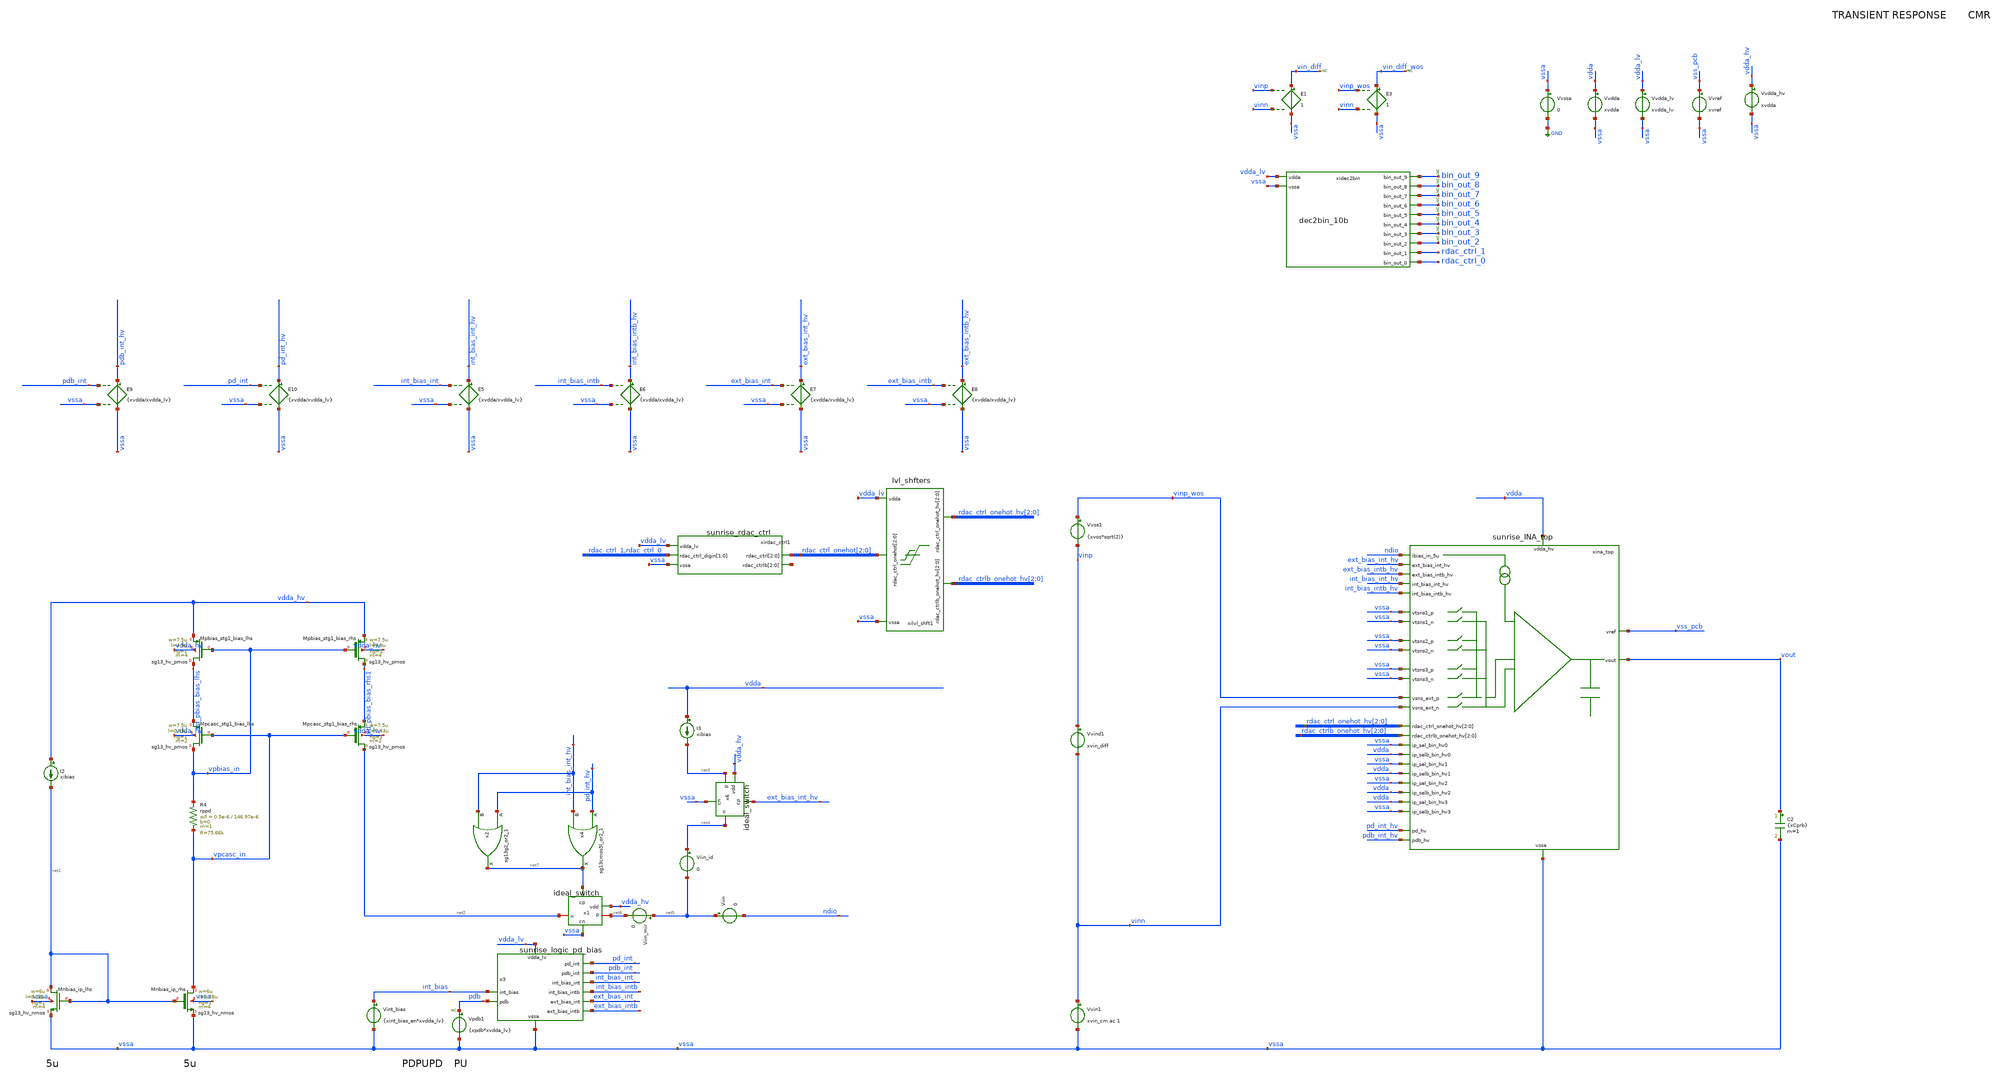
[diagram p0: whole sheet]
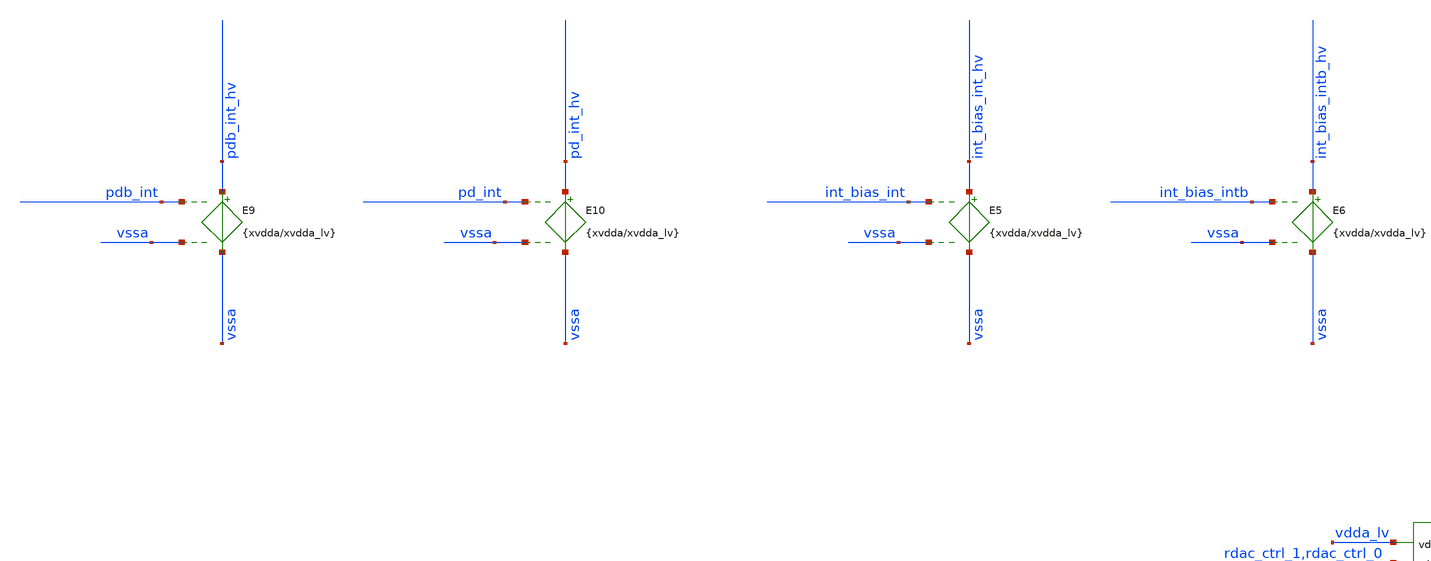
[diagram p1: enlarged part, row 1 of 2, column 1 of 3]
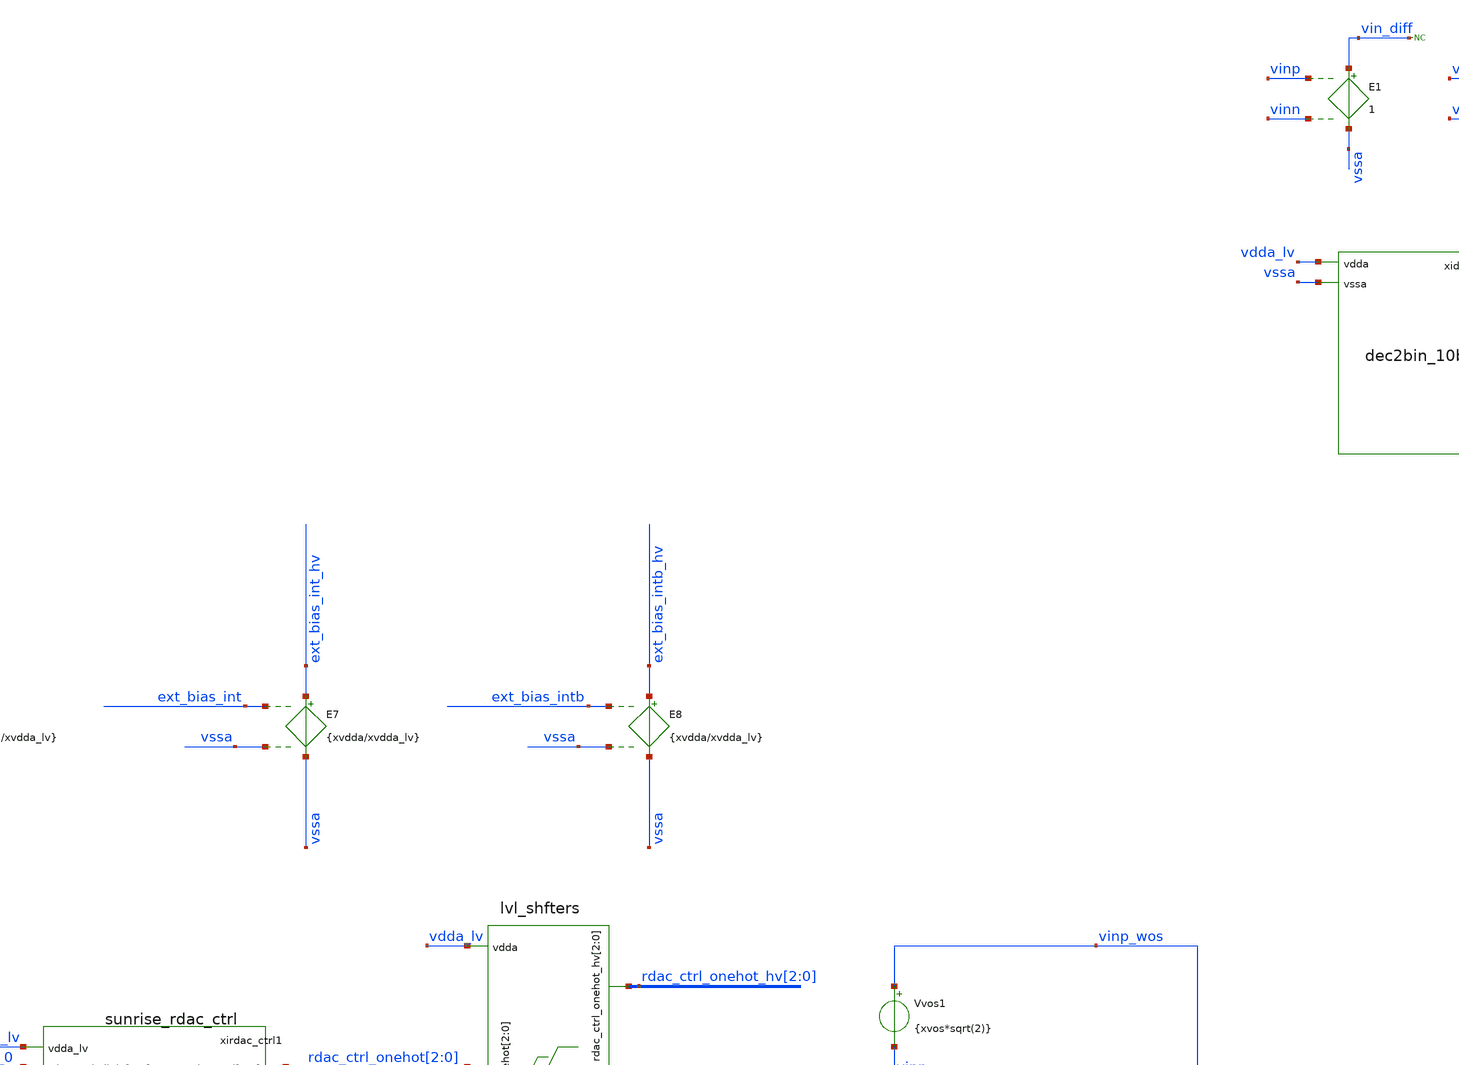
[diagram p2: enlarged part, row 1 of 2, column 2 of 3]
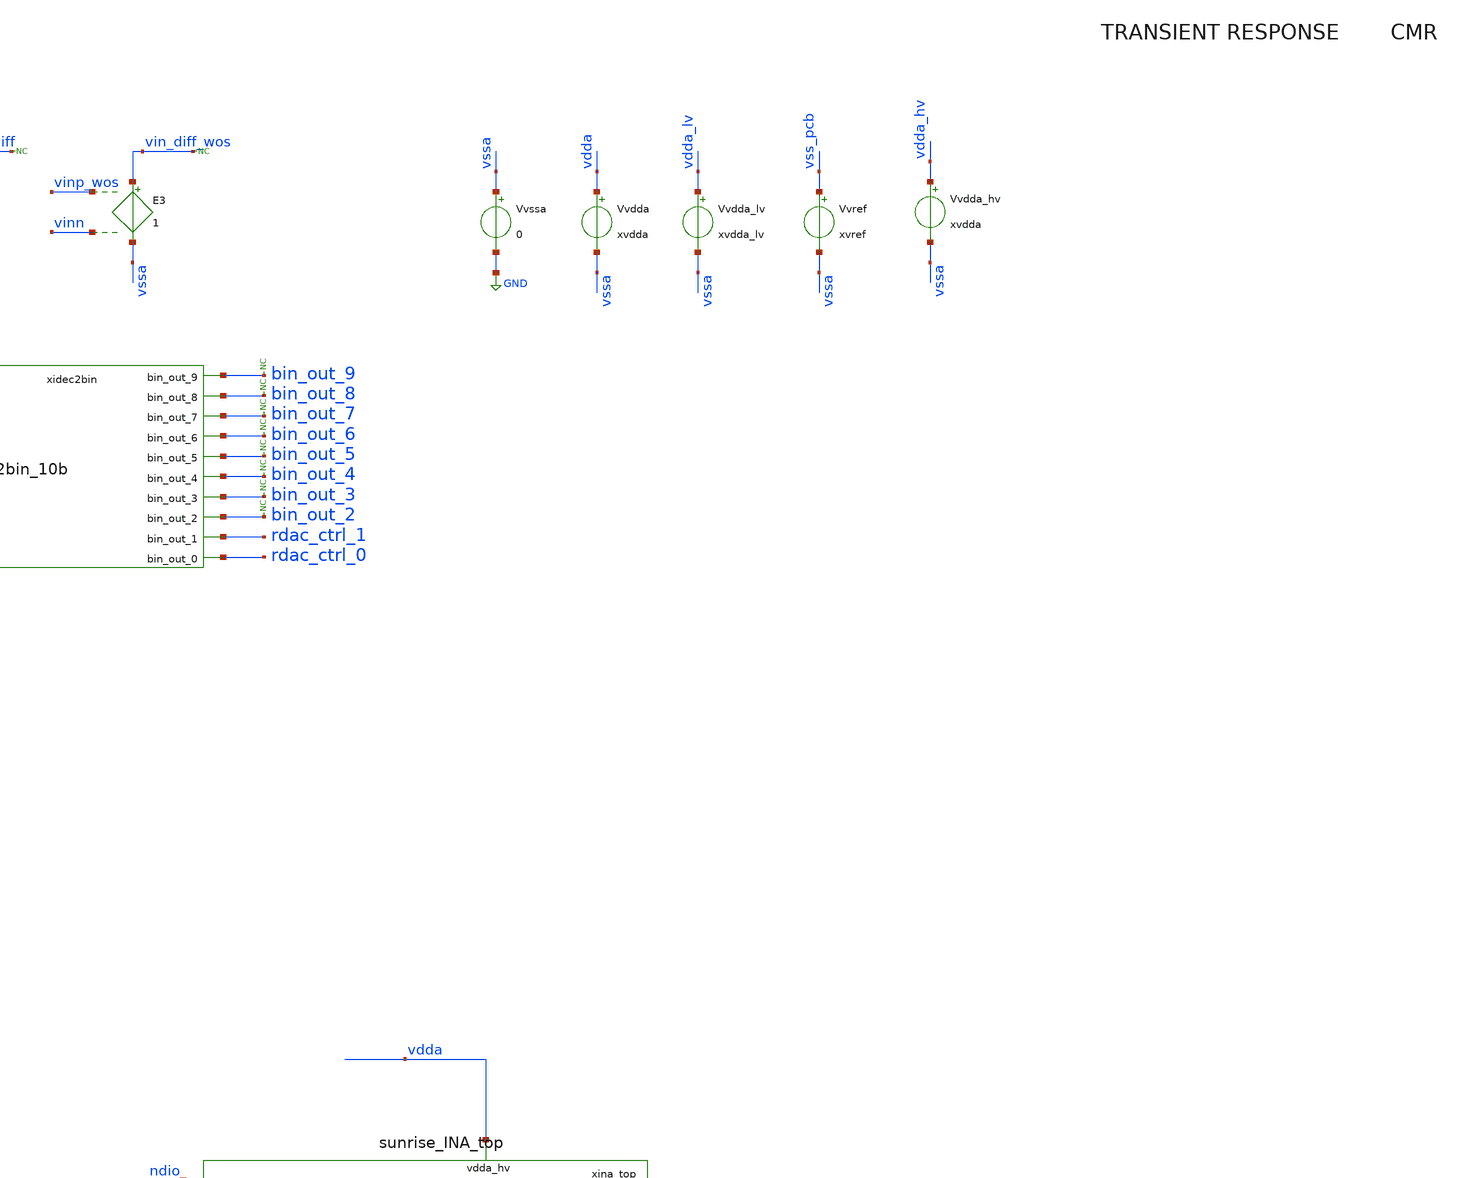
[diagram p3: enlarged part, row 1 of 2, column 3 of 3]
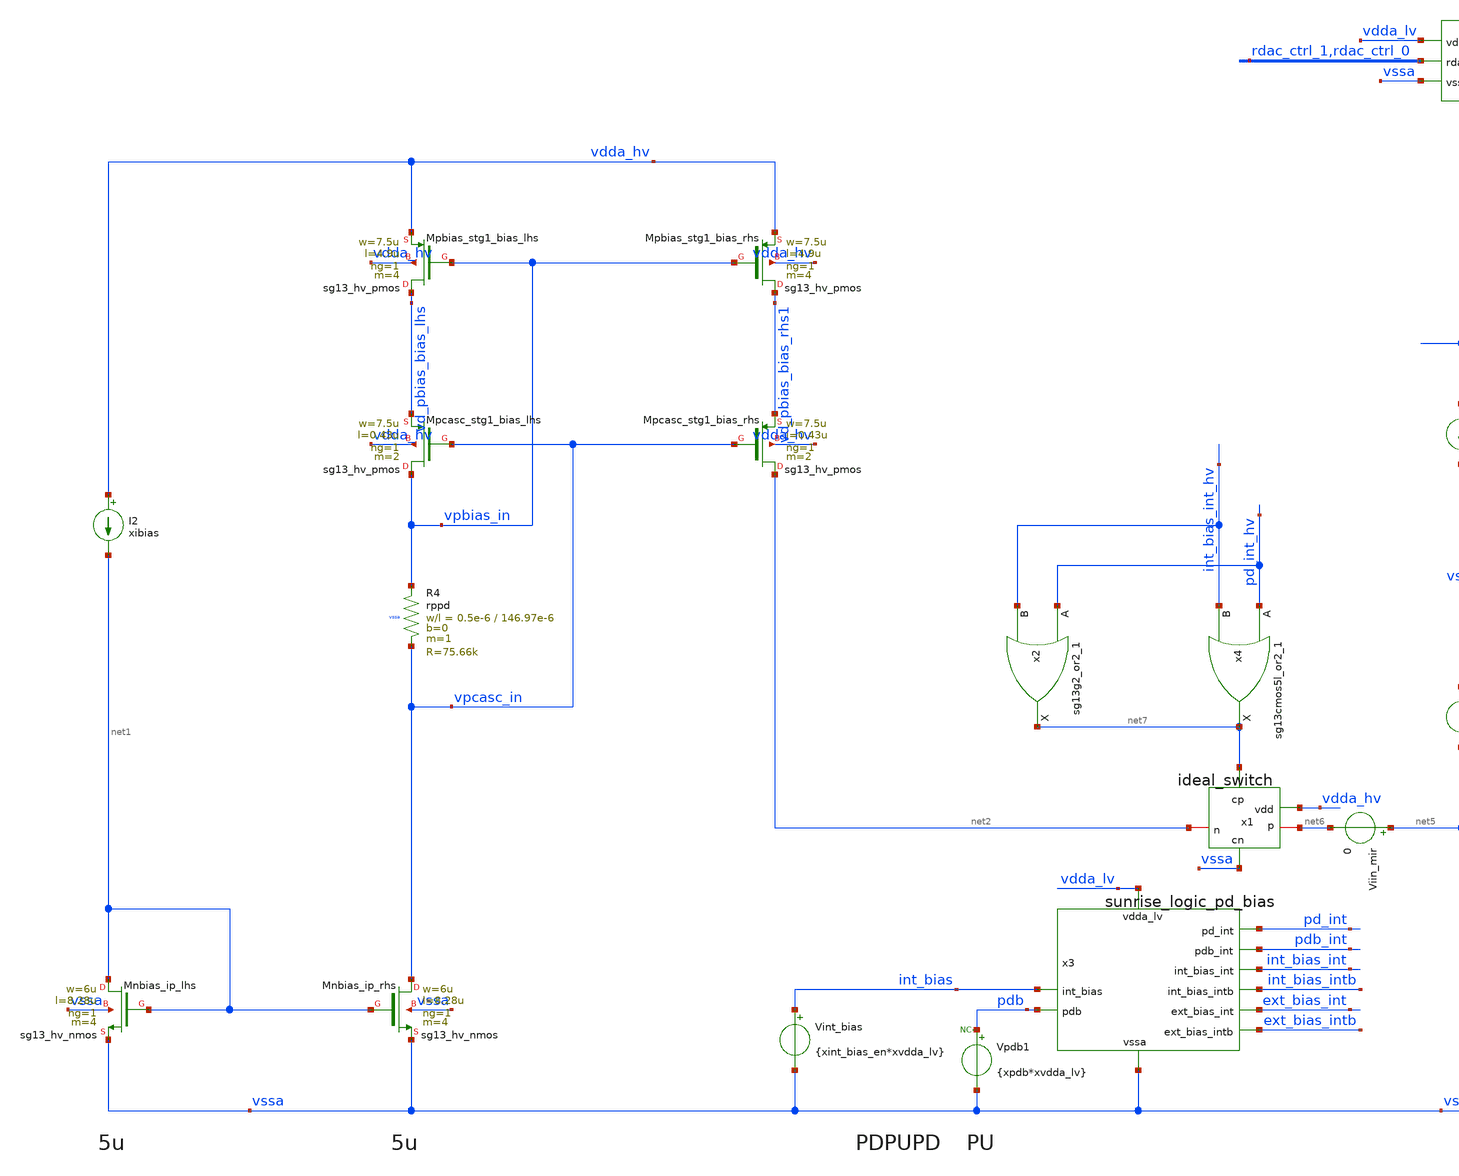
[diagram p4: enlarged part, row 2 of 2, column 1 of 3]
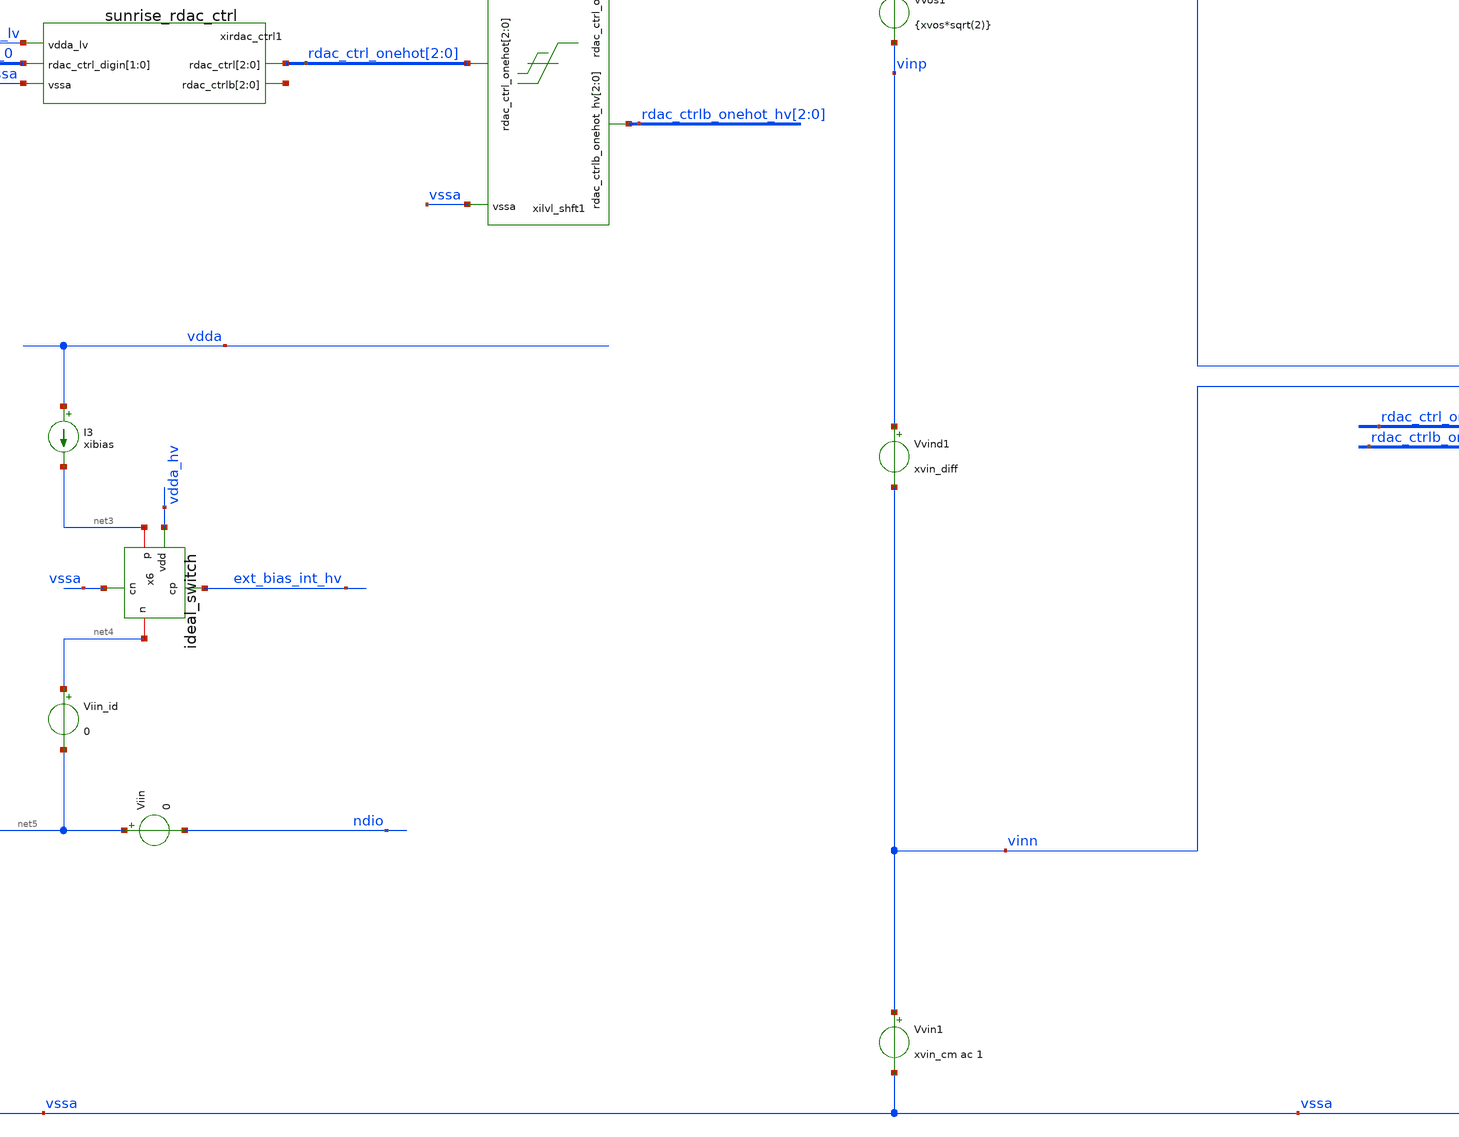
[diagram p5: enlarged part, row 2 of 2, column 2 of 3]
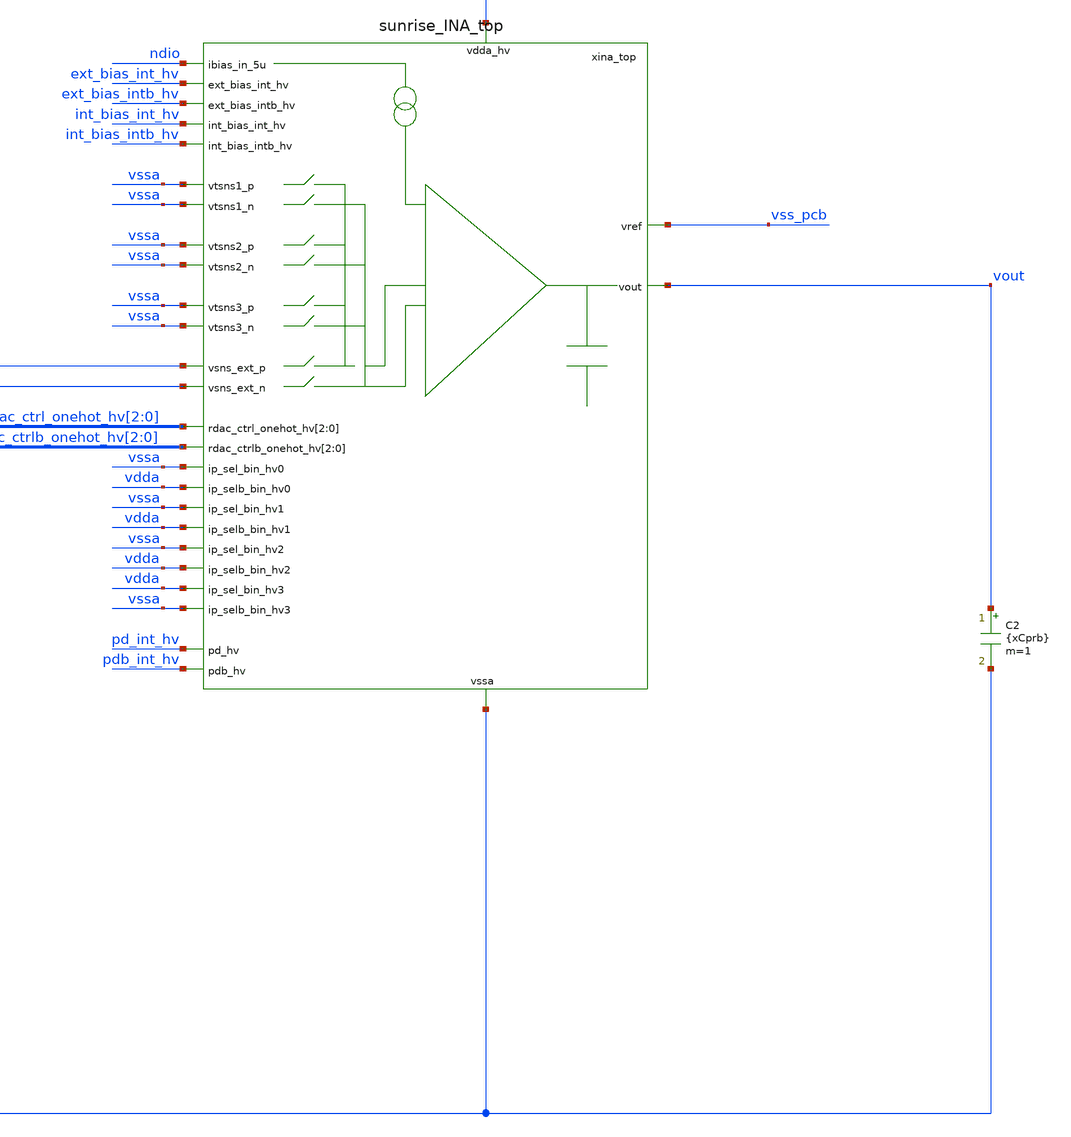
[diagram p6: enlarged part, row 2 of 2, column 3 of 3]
** sch_path: Design_Review_2/INA/Testbench_7_tb_sunrise_ina_top_CMR/tb_sunrise_ina_top_CMR.sch
**.subckt tb_sunrise_ina_top_CMR
Vvssa vssa GND 0
E1 vin_diff vssa vinp vinn 1
Vvref vss_pcb vssa xvref
* noconn vin_diff
E3 vin_diff_wos vssa vinp_wos vinn 1
* noconn vin_diff_wos
Vvdda_lv vdda_lv vssa xvdda_lv
xidec2bin bin_out_9 bin_out_8 bin_out_7 bin_out_6 bin_out_5 bin_out_4 bin_out_3 bin_out_2
+ rdac_ctrl_1 rdac_ctrl_0 vdda_lv vssa dec2bin_10b dec_code=dec_code_var
* noconn bin_out_9
* noconn bin_out_8
* noconn bin_out_7
* noconn bin_out_6
* noconn bin_out_5
* noconn bin_out_4
* noconn bin_out_3
* noconn bin_out_2
Vvdda vdda vssa xvdda
C2 vout vssa {xCprb} m=1
Vvin1 vinn vssa xvin_cm ac 1
Vvind1 vinp vinn xvin_diff
Vvos1 vinp_wos vinp {xvos*sqrt(2)}
xirdac_ctrl1 rdac_ctrl_1 rdac_ctrl_0 rdac_ctrl_onehot[2] rdac_ctrl_onehot[1] rdac_ctrl_onehot[0]
+ vdda_lv vssa net8[2] net8[1] net8[0] sunrise_rdac_ctrl
xilvl_shft1 rdac_ctrl_onehot[2] rdac_ctrl_onehot[1] rdac_ctrl_onehot[0] rdac_ctrlb_onehot_hv[2]
+ rdac_ctrlb_onehot_hv[1] rdac_ctrlb_onehot_hv[0] vssa rdac_ctrl_onehot_hv[2] rdac_ctrl_onehot_hv[1] rdac_ctrl_onehot_hv[0]
+ vdda_lv lvl_shfters
XMnbias_ip_lhs net1 net1 vssa vssa sg13_hv_nmos w=6u l=8.28u ng=1 m=4 mm_ok=1
XMnbias_ip_rhs vpcasc_in net1 vssa vssa sg13_hv_nmos w=6u l=8.28u ng=1 m=4 mm_ok=1
XMpcasc_stg1_bias_lhs vpbias_in vpcasc_in vd_pbias_bias_lhs vdda_hv sg13_hv_pmos w=7.5u l=0.43u ng=1
+ m=2 mm_ok=1
XMpbias_stg1_bias_lhs vd_pbias_bias_lhs vpbias_in vdda_hv vdda_hv sg13_hv_pmos w=7.5u l=4.9u ng=1
+ m=4 mm_ok=1
XMpcasc_stg1_bias_rhs net2 vpcasc_in vd_pbias_bias_rhs1 vdda_hv sg13_hv_pmos w=7.5u l=0.43u ng=1 m=2
+ mm_ok=1
XMpbias_stg1_bias_rhs vd_pbias_bias_rhs1 vpbias_in vdda_hv vdda_hv sg13_hv_pmos w=7.5u l=4.9u ng=1
+ m=4 mm_ok=1
XR4 vpbias_in vpcasc_in vssa rppd w=0.5e-6 l=146.97e-6 m=1 b=0 mm_ok=1
I2 vdda_hv net1 xibias
I3 vdda net3 xibias
Vint_bias int_bias vssa {xint_bias_en*xvdda_lv}
x6 vdda_hv ext_bias_int_hv net3 net4 vssa ideal_switch
x1 vdda_hv net7 net6 net2 vssa ideal_switch
Viin_id net4 net5 0
Viin_mir net5 net6 0
Viin net5 ndio 0
x2 net7 pd_int_hv int_bias_int_hv vdda_hv vssa sg13g2_or2_1
Vpdb1 pdb vssa {xpdb*xvdda_lv}
* noconn pdb
x3 vdda_lv vssa int_bias_intb int_bias int_bias_int pdb ext_bias_intb ext_bias_int pdb_int pd_int
+ sunrise_logic_pd_bias
E5 int_bias_int_hv vssa int_bias_int vssa {xvdda/xvdda_lv}
E6 int_bias_intb_hv vssa int_bias_intb vssa {xvdda/xvdda_lv}
E7 ext_bias_int_hv vssa ext_bias_int vssa {xvdda/xvdda_lv}
E8 ext_bias_intb_hv vssa ext_bias_intb vssa {xvdda/xvdda_lv}
E9 pdb_int_hv vssa pdb_int vssa {xvdda/xvdda_lv}
E10 pd_int_hv vssa pd_int vssa {xvdda/xvdda_lv}
Vvdda_hv vdda_hv vssa xvdda
xina_top vssa vssa vdda vssa vssa ndio ext_bias_int_hv vssa ext_bias_intb_hv int_bias_int_hv vss_pcb
+ int_bias_intb_hv vssa vinp_wos vout vinn rdac_ctrl_onehot_hv[2] rdac_ctrl_onehot_hv[1] rdac_ctrl_onehot_hv[0]
+ rdac_ctrlb_onehot_hv[2] rdac_ctrlb_onehot_hv[1] rdac_ctrlb_onehot_hv[0] vssa vdda pd_int_hv pdb_int_hv vssa vssa vdda vssa
+ vdda vdda vssa sunrise_INA_top
x4 net7 pd_int_hv int_bias_int_hv vdda_hv vssa sg13cmos5l_or2_1
**** begin user architecture code

** opencircuitdesign pdks install
** STD CORNERS **
.lib /home/slice/pdk/iHP/IHP-Open-PDK/ihp-sg13g2/libs.tech/ngspice/models/cornerMOSlv.lib mos_tt
.lib /home/slice/pdk/iHP/IHP-Open-PDK/ihp-sg13g2/libs.tech/ngspice/models/cornerMOShv.lib mos_tt
.lib /home/slice/pdk/iHP/IHP-Open-PDK/ihp-sg13g2/libs.tech/ngspice/models/cornerRES.lib res_typ
* SG13G2 STD CELLS
*.include /home/slice/pdk/iHP/IHP-Open-PDK/ihp-sg13g2/libs.ref/sg13g2_stdcell/spice/sg13g2_stdcell.spice
* SG13CMOS5L STD CELLS
.include /home/slice/pdk/iHP/IHP-Open-PDK/ihp-sg13cmos5l/libs.ref/sg13cmos5l_stdcell/spice/sg13cmos5l_stdcell.spice

** MC CORNERS **
*.lib /home/slice/pdk/iHP/IHP-Open-PDK/ihp-sg13g2/libs.tech/ngspice/models/cornerMOShv.lib mos_tt_mismatch
*.lib /home/slice/pdk/iHP/IHP-Open-PDK/ihp-sg13g2/libs.tech/ngspice/models/cornerMOShv.lib mos_ss_mismatch
*.lib /home/slice/pdk/iHP/IHP-Open-PDK/ihp-sg13g2/libs.tech/ngspice/models/cornerMOShv.lib mos_ff_mismatch
*.lib /home/slice/pdk/iHP/IHP-Open-PDK/ihp-sg13g2/libs.tech/ngspice/models/cornerRES.lib res_typ_mismatch
*.lib /home/slice/pdk/iHP/IHP-Open-PDK/ihp-sg13g2/libs.tech/ngspice/models/cornerRES.lib res_bcs_mismatch
*.lib /home/slice/pdk/iHP/IHP-Open-PDK/ihp-sg13g2/libs.tech/ngspice/models/cornerRES.lib res_wcs_mismatch

** SIMULATOR ENGINE SETUP **
.options method = gear
.options ABSTOL = 1e-12
.options RELTOL = 1e-4
.options VNTOL = 1e-9
.options TRTOL = 7
.options GMIN = 1e-12
.options interp $ interpolates output data onto fixed time steps on a TSTEP grid

** PARAMETERS **

* global parameters
.param xvdda = 3.3
.param xvdda_lv = 1.5
.param xtsim = 2u
.csparam xtsim_var = 'xtsim'
.param xibias = 5u
.param xCload = 0p
.param xCfilt = 5p
.param xCprb = 20p
.param xtstep = 100n
*.param xtrf = 1n
.csparam xtstep_var = 'xtstep'
.param xdc_step = 10m
.csparam xdc_step_var = 'xdc_step'
.param xvos = 0m
.param xint_bias_en = 0
* active lo => 0 = pd
.param xpdb = 1
.param xnoise_stg1 = 1
.param xnoise_stg1_ia = 1
.param xnoise_stg1_nia = 1
.param xnoise_stg1_rg = 1
.param xnoise_stg2 = 1

* input swing parameters
* Below assumes you want a full input swing
* this is the margin between the supplies which vout can swing to
.param xvmargin = 50m
* max vout
.param xvin_diff_for_vout_max = (xvdda-(2*xvmargin))/xAv_ina
.csparam xvin_diff_for_vout_max_var = 'xvin_diff_for_vout_max'
* min vout
.param xvin_diff_for_vout_min =  (xvmargin/xAv_ina)
.csparam xvin_diff_for_vout_min_var = 'xvin_diff_for_vout_min'

* set xvin_diff according to desired vout (max or min)
*.param xvin_diff = xvin_diff_for_vout_max

* note on vin_cm: vin_cm_min = max(1V,xAv_ia*vd_max).
* The 1V is due to the NMOS dp and means you cant sense < 1V.
* If you set vcm = xAv_ia*vd_max (assuming this is > 1V),
* you will get a full signal swing at the input (=xvdda/xAv_ina).
* If vcm gets larger, the NIA starts to saturate so dvin needs to be
* be < xvdda/xAv_ina. vin_cm_max simply equals xvdda.
*.param xvin_cm = xAv_ia*(xvdda/xAv_ina)
.param xvin_cm = (xAv_ia*((xvdda-(2*xvmargin))/xAv_ina))+xvmargin

* Below assumes you want to pick specific values
*.param xvin_cm = xvdda/2+0m
.csparam xvin_cm_var = 'xvin_cm'
.param xvin_diff = 0m
.csparam xvin_diff_var = 'xvin_diff'

* set to the below to measure offset
*.param xvin_diff = 0

* ota model parameters
.param xAv0_dB = 70
.param xAv0 = 10^(xAv0_dB/20)
.param xgmdp = 1m
.param xGBW = 1Meg

* stg1 parameters
* Av = 1 => xRg = 50G, Av = 5 => xRg = 50k, Av = 11 => xRg = 20k, Av = 21 => xRg = 10k
.param xRg= 50k
.param dec_code_var = 1
.csparam xdec_code_var = 'dec_code_var'
* below is to ensure gain error due to xRsw < 1%
*.param xRsw = xRg/100
* below is to manually enter a value for xRsw
.param xRsw = 100
.param xRfb_stg1 = 100k
.param xAv_stg1 = 1+((2*xRfb_stg1)/xRg)
.csparam xAv_stg1_var = 'xAv_stg1'
.param xbeta_stg1 = 1/xAv_stg1
.param lg_stg1 = xAv0*xbeta_stg1
.csparam lg_stg1_var = 'lg_stg1'
.param xAv_ia = xRfb_stg1/xRg

* stg2 parameters
.param xvref = 3.3/2
.param xRin_stg2 = 10k
.param xRfb_stg2 = 10k
.param xAv_stg2 = xRfb_stg2/xRin_stg2
.csparam xAv_stg2_var = 'xAv_stg2'
.param xbeta_stg2 = xRin_stg2/(xRin_stg2+xRfb_stg2)
.param lg_stg2 = xAv0*xbeta_stg2
.csparam lg_stg2_var = 'lg_stg2'

* total ina gain parameter
.param xAv_ina = xAv_stg1*xAv_stg2
.csparam xAv_ina_var = 'xAv_ina'

.temp 27

* vlogA instantiations
.model OTA_vcvs OTA_vcvs
.model ideal_sw ideal_sw
.model dec2bin_10b dec2bin_10b

.include tb_sunrise_ina_top_CMR.save

* below line needs to be included if running ac noise analysys
*.save all
.save v(vout)

*.option savecurrents

*.save onoise* inoise* frequency
*.save i(v.xstb.Vi) v(xstb.x) v(av)
*.save v(vinp) v(vinn) v(vinp_wos) v(vin_diff) v(vin_diff_wos) v(vfb_ni) v(vfb_i) v(vih) v(vil) v(vip_stg2) v(vin_stg2) v(vin_stg2_diff) v(vout)
*.save v(vdda) v(vdda_lv) v(vssa) v(vss_pcb) v(ibias1) v(ibias2) v(ibias3) v(vfb_ni2) v(vfb_i2) v(rdac_ctrl_1) v(rdac_ctrl_0)
*.save v(xirdac.xirdac_ctrl.rdac_ctrl_int[0]) v(xirdac.xirdac_ctrl.rdac_ctrlb_int[0]) v(xirdac.xirdac_ctrl.rdac_ctrl_int[1]) v(xirdac.xirdac_ctrl.rdac_ctrlb_int[1]) v(xirdac.rdac_ctrl_onehot[2]) v(xirdac.rdac_ctrl_onehot[1]) v(xirdac.rdac_ctrl_onehot[0]) v(xirdac.rdac_ctrl_onehot_hv[2]) v(xirdac.rdac_ctrl_onehot_hv[1]) v(xirdac.rdac_ctrl_onehot_hv[0]) v(xirdac.rdac_ctrlb_onehot_hv[2]) v(xirdac.rdac_ctrlb_onehot_hv[1]) v(xirdac.rdac_ctrlb_onehot_hv[0])

.control

pre_osdi OTA_vcvs.osdi
pre_osdi ideal_sw.osdi
pre_osdi dec2bin_10b.osdi

 * commercial temperature range
 *set xTj = ( 0 10 20 30 40 50 60 70 )
 * industrial temperature range
 *set xTj = ( -40 -30 -20 -10 0 10 20 30 40 50 60 70 85 )
 * military temperature range
 *set xTj = ( -55 -40 -30 -20 -10 0 10 20 30 40 50 60 70 80 90 100 110 125 )
 * automotive temperature range
 *set xTj = ( -40 -30 -20 -10 0 10 20 30 40 50 60 70 80 90 100 110 120 130 140 150 )
 set xTj = ( 27 )

   foreach xTj_var $xTj

   let Tj_meas = $xTj_var

   echo temperature is "$&Tj_meas"

   set temp = $xTj_var

   echo vin_cm is "$&xvin_cm_var"
   echo vin_diff is "$&xvin_diff_var"
   echo tstep is "$&xtstep_var"

   let run = 1

  dowhile run <= 1
  reset

** 1. DCOP ANALYSIS (comment out for MC analysis to speed up sims) **

  *op
  *remzerovec
  *set filetype=binary
  ** first write deletes existing file
  * comment out to save space for MC analysis
  *write tb_sunrise_ina_dcop.raw

** 2. TRAN ANALYSIS **


  **set appendwrite
  tran $&xtstep_var $&xtsim_var
  remzerovec
  * comment out to save space for MC analysis
  write tb_sunrise_ina_tran.raw
  **unset appendwrite
  option

** 3. TRAN MEASURES **
   meas tran vout_ave AVG v(vout) from=1n to=$&xtsim_var
   echo "$&vout_ave" >> vout_v.txt

** 4. AC ANALYSIS **

  ac dec 10 1 1G

  *remzerovec
  *write tb_sunrise_ina_ac.raw

** 5. CMR ANALYSIS **

  meas AC CMR_DC_dB FIND vdb(vout) AT=10
  echo --
  echo  CMR_DC_dB = "$&CMR_DC_dB"
  echo "$&CMR_DC_dB" >> CMR_DC_dB.txt
  echo --
  let CMR_DC_lin = 10^($&CMR_DC_dB/20)
  echo CMR_DC_lin = "$&CMR_DC_lin"
  echo "$&CMR_DC_lin" >> CMR_DC_lin.txt
  echo --
  echo Av_ina = "$&xAv_ina_var"
  let Av_ina_dB = 20*log10($&xAv_ina_var)
  echo Av_ina_dB = "$&Av_ina_dB"
  echo --
  let CMRR_DC_lin = $&CMR_DC_lin/$&xAv_ina_var
  echo CMRR_DC_lin = "$&CMRR_DC_lin"
  echo "$&CMRR_DC_lin" >> CMRR_DC_lin.txt
  echo --
  let CMRR_DC_db = 20*log10($&CMRR_DC_lin)
  echo CMRR_DC_db = "$&CMRR_DC_db"
  echo "$&CMRR_DC_dB" >> CMRR_DC_dB.txt
  echo --

  remzerovec
  set filetype=binary
  ** first write deletes existing file
  * comment out to save space for MC analysis
  write tb_sunrise_ina_ac_mc.raw
  ** set appendwrite appends following writes to existing raw file
  set appendwrite
  let run = run+1

  end
  end

  setplot
*quit 0
.endc




**** end user architecture code
**.ends
.GLOBAL GND
.end
